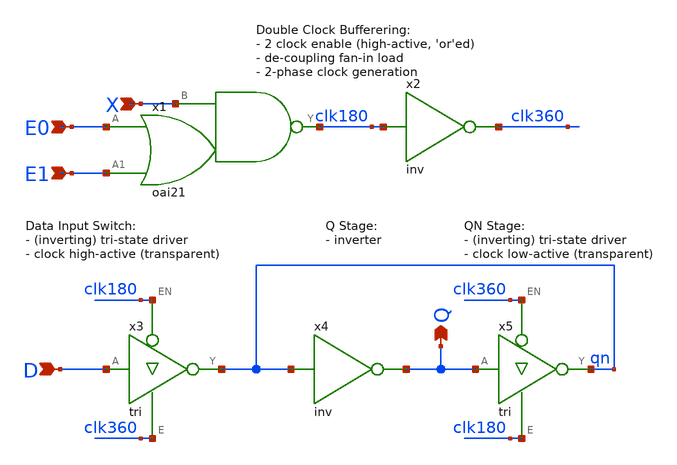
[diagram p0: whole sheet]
** sch_path: Sources/crafted/LATEEP.sch
**.subckt LATEEP X D Q E0 E1
*.ipin X
*.ipin D
*.opin Q
*.ipin E0
*.ipin E1
x2 clk180 clk360 VDD GND inv Wmin=1.5u Lmin=1u g=2 m=1
x4 qn Q VDD GND inv Wmin=1.5u Lmin=1u g=2 m=1
x3 D clk180 clk360 qn VDD GND tri Wmin=1.5u Lmin=1u g=2 m=1
x5 Q clk360 clk180 qn VDD GND tri Wmin=1.5u Lmin=1u g=2 m=1
x1 E0 E1 clk180 X VDD GND oai21 Wmin=1.5u Lmin=1u g=2 m=1
**.ends
.end
